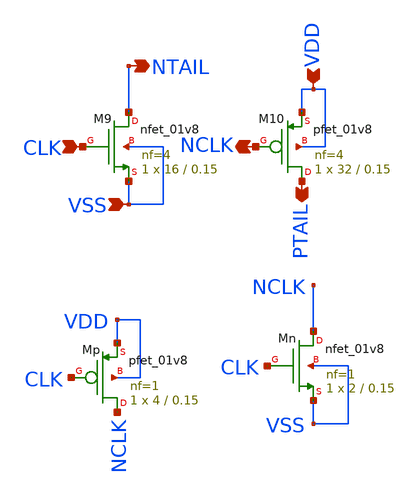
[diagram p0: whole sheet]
** sch_path: strongarm_clock.sch
**.subckt strongarm_clock CLK NCLK NTAIL PTAIL VDD VSS
*.ipin CLK
*.opin NCLK
*.opin NTAIL
*.opin PTAIL
*.ipin VDD
*.ipin VSS
XM10 PTAIL NCLK VDD VDD sky130_fd_pr__pfet_01v8 L=0.15 W=32 nf=4 ad='int((4 + 1)/2) * 32 / 4 * 0.29'
+ as='int((4 + 2)/2) * 32 / 4 * 0.29' pd='2*int((4 + 1)/2) * (32 / 4 + 0.29)' ps='2*int((4 + 2)/2) * (32 / 4 + 0.29)'
+ nrd='0.29 / 32 ' nrs='0.29 / 32 ' sa=0 sb=0 sd=0 mult=1 m=1
XM9 NTAIL CLK VSS VSS sky130_fd_pr__nfet_01v8 L=0.15 W=16 nf=4 ad='int((4 + 1)/2) * 16 / 4 * 0.29' as='int((4 + 2)/2) * 16 / 4 * 0.29'
+ pd='2*int((4 + 1)/2) * (16 / 4 + 0.29)' ps='2*int((4 + 2)/2) * (16 / 4 + 0.29)' nrd='0.29 / 16 ' nrs='0.29 / 16 '
+ sa=0 sb=0 sd=0 mult=1 m=1
XMp NCLK CLK VDD VDD sky130_fd_pr__pfet_01v8 L=0.15 W=4 nf=1 ad='int((1 + 1)/2) * 4 / 1 * 0.29' as='int((1 + 2)/2) * 4 / 1 * 0.29'
+ pd='2*int((1 + 1)/2) * (4 / 1 + 0.29)' ps='2*int((1 + 2)/2) * (4 / 1 + 0.29)' nrd='0.29 / 4 ' nrs='0.29 / 4 '
+ sa=0 sb=0 sd=0 mult=1 m=1
XMn NCLK CLK VSS VSS sky130_fd_pr__nfet_01v8 L=0.15 W=2 nf=1 ad='int((1 + 1)/2) * 2 / 1 * 0.29' as='int((1 + 2)/2) * 2 / 1 * 0.29'
+ pd='2*int((1 + 1)/2) * (2 / 1 + 0.29)' ps='2*int((1 + 2)/2) * (2 / 1 + 0.29)' nrd='0.29 / 2 ' nrs='0.29 / 2 '
+ sa=0 sb=0 sd=0 mult=1 m=1
**.ends
.end
